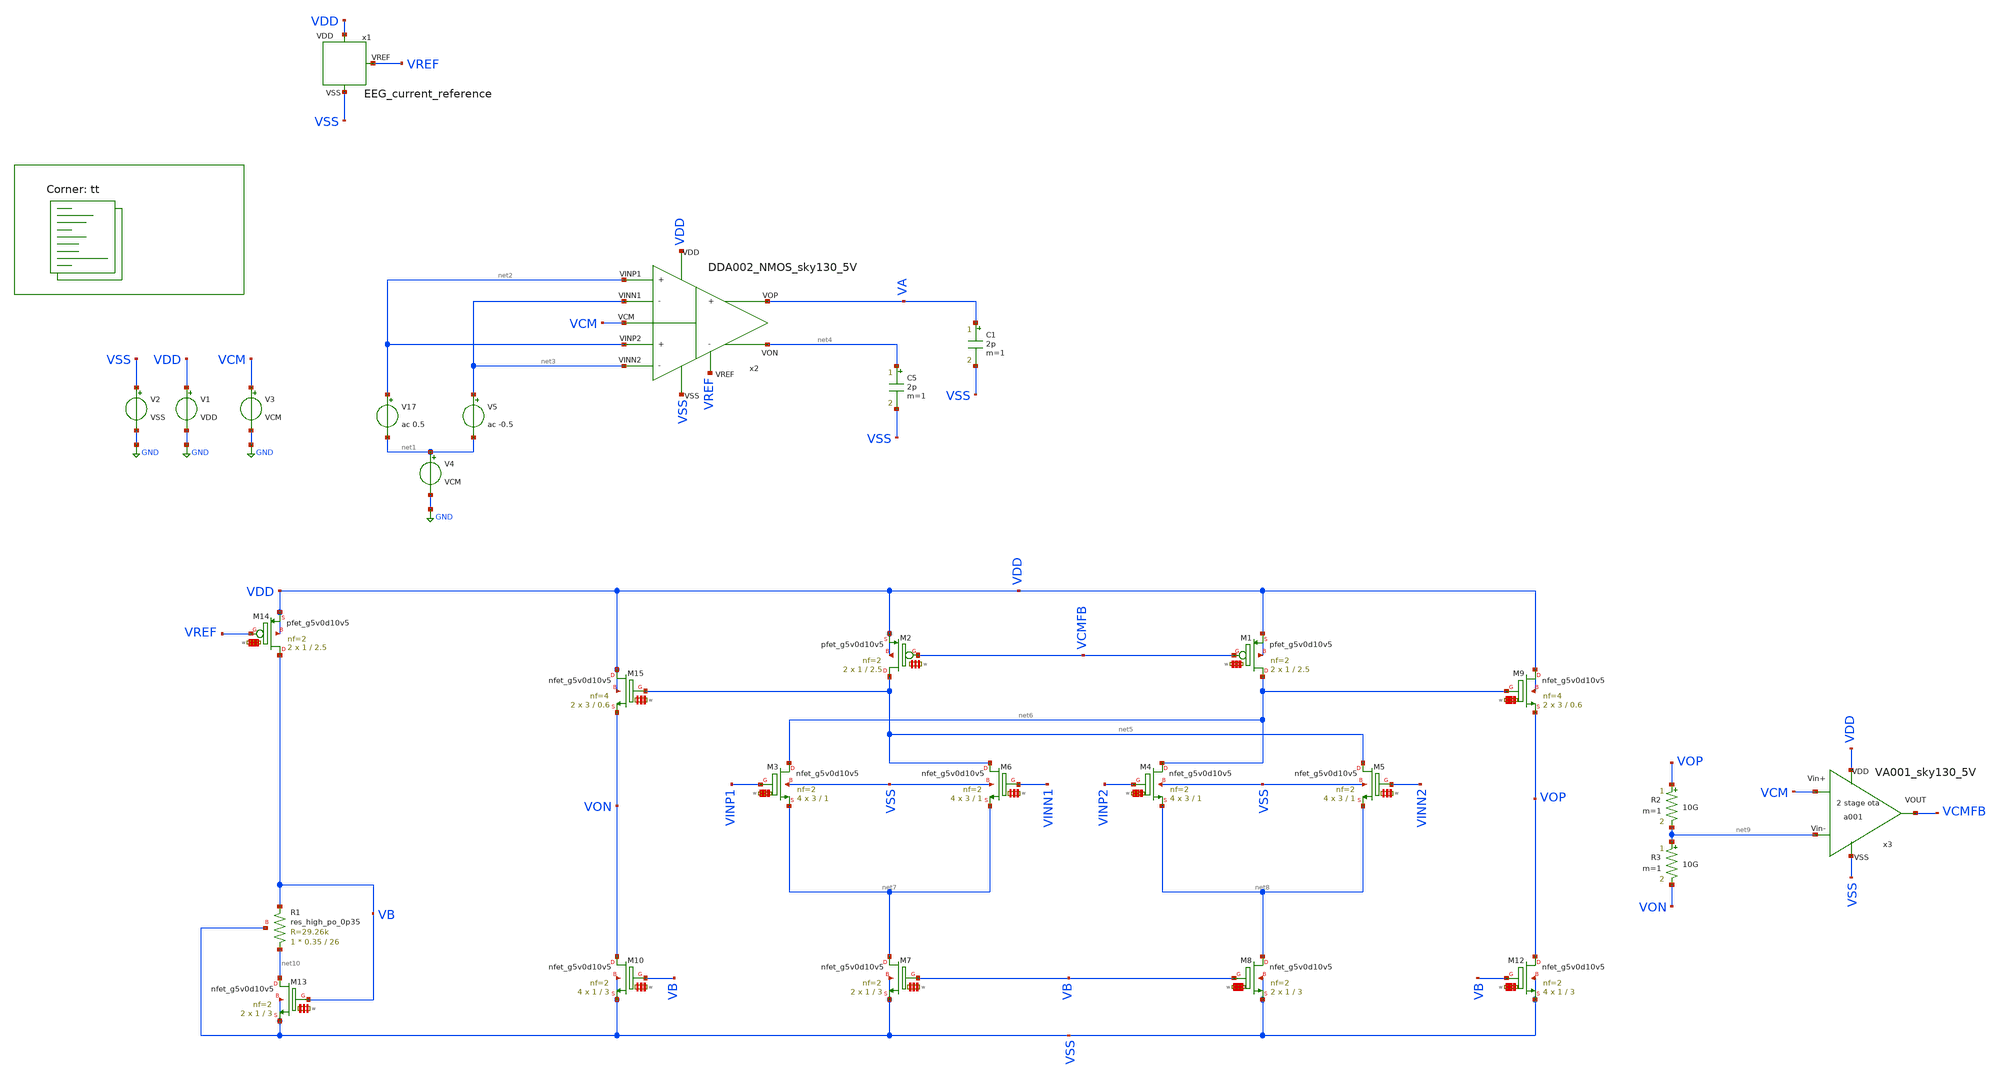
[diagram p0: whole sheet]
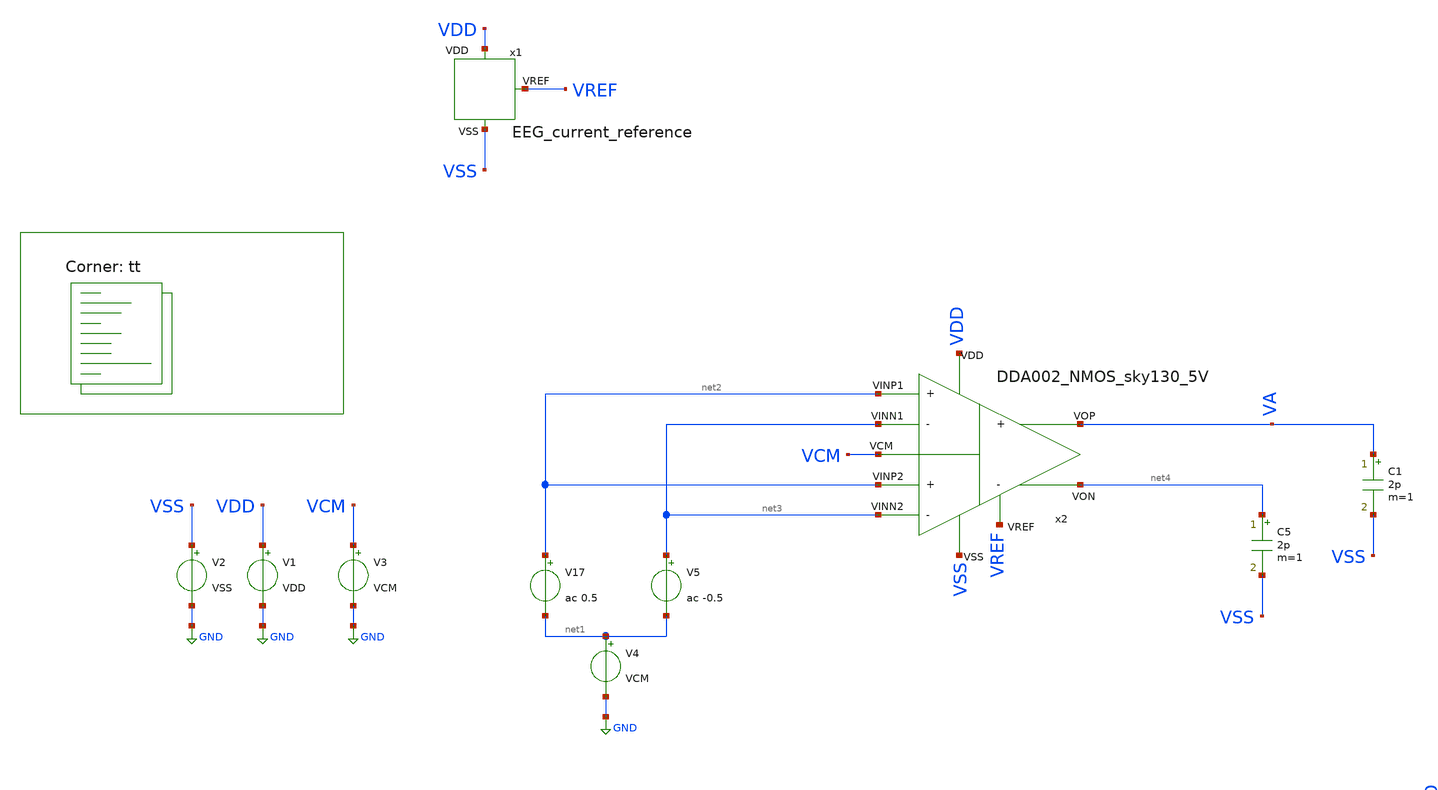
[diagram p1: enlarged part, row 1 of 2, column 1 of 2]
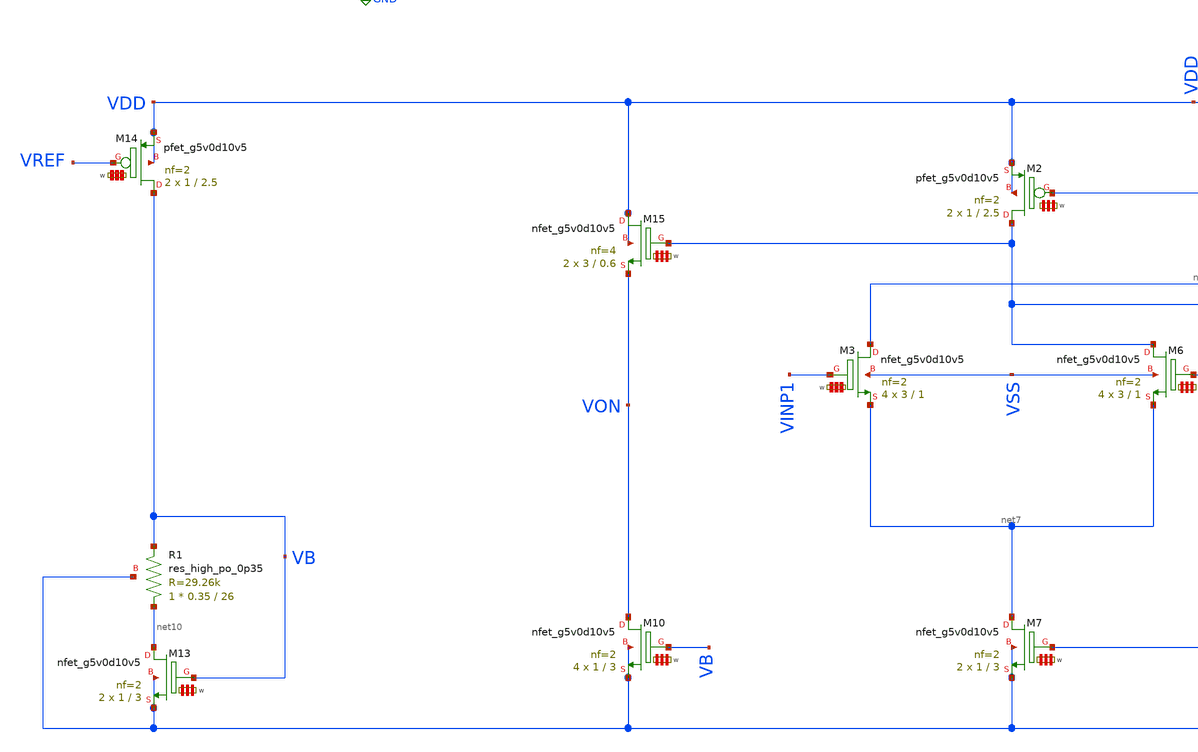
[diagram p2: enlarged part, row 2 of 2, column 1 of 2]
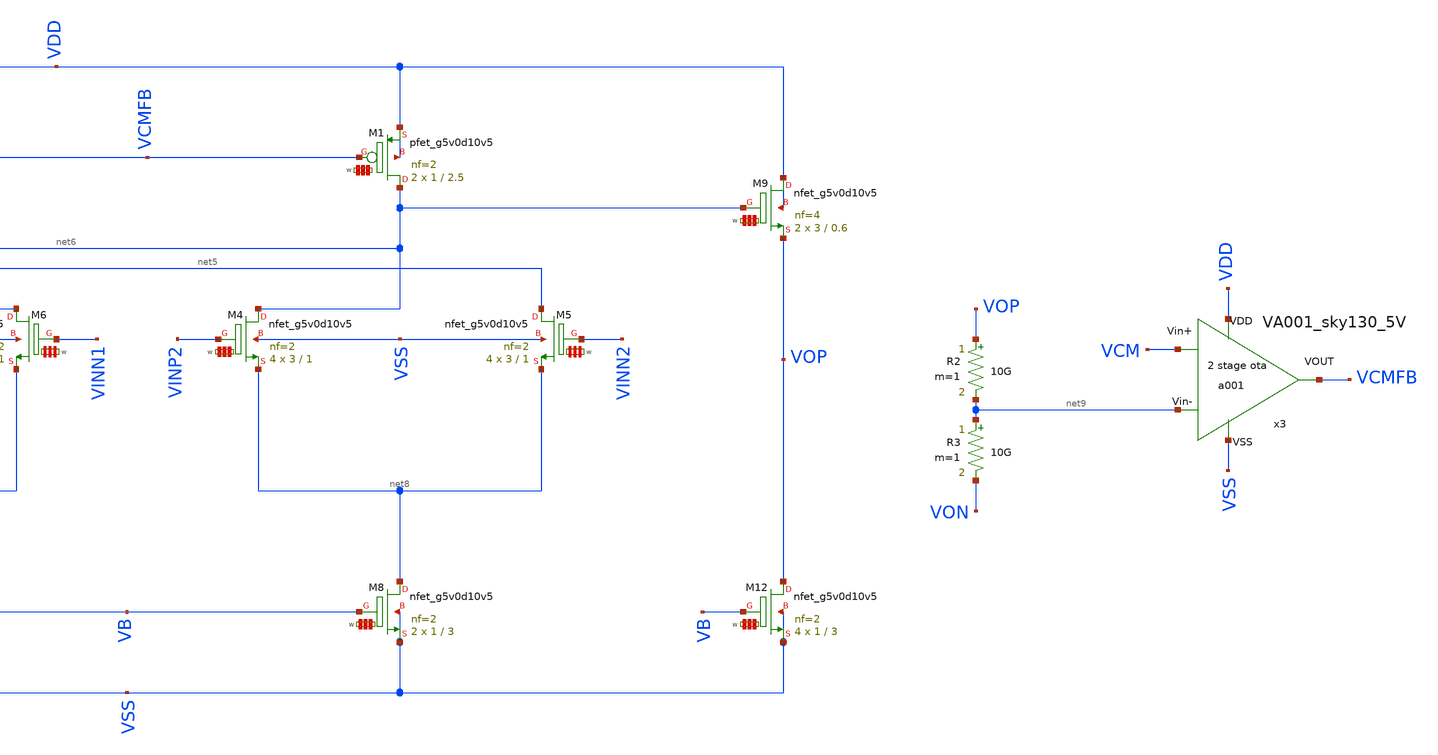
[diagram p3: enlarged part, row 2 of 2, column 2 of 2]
** sch_path: Learning/complex_projects/A_Two-Stage_Time_Division_Multiplexing_AFE_with_Input_Impedance_Boosting_DDA_for_EEG_Signal_Acquisition/sky130A_5V/input_buffer_chopper/DDA_TB.sch
**.subckt DDA_TB
V1 VDD GND VDD
V2 VSS GND VSS
x1 VDD VSS VREF EEG_current_reference
x2 VDD VSS VREF net3 net3 net2 net2 VCM VA net4 DDA002_NMOS_sky130_5V
V3 VCM GND VCM
V4 net1 GND VCM
V17 net2 net1 ac 0.5
V5 net3 net1 ac -0.5
C5 net4 VSS 2p m=1
C1 VA VSS 2p m=1
XM2 net5 VCMFB VDD VDD sky130_fd_pr__pfet_g5v0d10v5 L=2.5 W='1 * 2 ' nf=2 ad='int((2 + 1)/2) * 1 * 0.29'
+ as='int((2 + 2)/2) * 1 * 0.29' pd='2*int((2 + 1)/2) * (1 + 0.29)' ps='2*int((2 + 2)/2) * (1 + 0.29)'
+ nrd='0.29 / 1 / 2 ' nrs='0.29 / 1 / 2 ' sa=0 sb=0 sd=0 mult=2 m=2
XM3 net6 VINP1 net7 VSS sky130_fd_pr__nfet_g5v0d10v5 L=1 W='3 * 2 ' nf=2 ad='int((nf+1)/2) * W / nf * 0.29'
+ as='int((nf+2)/2) * W / nf * 0.29' pd='2*int((nf+1)/2) * (W / nf + 0.29)' ps='2*int((nf+2)/2) * (W / nf + 0.29)'
+ nrd='0.29 / W ' nrs='0.29 / W ' sa=0 sb=0 sd=0 mult=4 m=4
x3 VDD VSS VCM net9 VCMFB VA001_sky130_5V
R2 VOP net9 10G m=1
R3 net9 VON 10G m=1
XM13 net10 VB VSS VSS sky130_fd_pr__nfet_g5v0d10v5 L=3 W='1 * 2 ' nf=2 ad='int((nf+1)/2) * W / nf * 0.29'
+ as='int((nf+2)/2) * W / nf * 0.29' pd='2*int((nf+1)/2) * (W / nf + 0.29)' ps='2*int((nf+2)/2) * (W / nf + 0.29)'
+ nrd='0.29 / W ' nrs='0.29 / W ' sa=0 sb=0 sd=0 mult=2 m=2
XR1 net10 VB VSS sky130_fd_pr__res_high_po_0p35 L=26 mult=1 m=1
XM14 VB VREF VDD VDD sky130_fd_pr__pfet_g5v0d10v5 L=2.5 W='1 * 2 ' nf=2 ad='int((2 + 1)/2) * 1 * 0.29'
+ as='int((2 + 2)/2) * 1 * 0.29' pd='2*int((2 + 1)/2) * (1 + 0.29)' ps='2*int((2 + 2)/2) * (1 + 0.29)'
+ nrd='0.29 / 1 / 2 ' nrs='0.29 / 1 / 2 ' sa=0 sb=0 sd=0 mult=2 m=2
XM7 net7 VB VSS VSS sky130_fd_pr__nfet_g5v0d10v5 L=3 W='1 * 2 ' nf=2 ad='int((nf+1)/2) * W / nf * 0.29'
+ as='int((nf+2)/2) * W / nf * 0.29' pd='2*int((nf+1)/2) * (W / nf + 0.29)' ps='2*int((nf+2)/2) * (W / nf + 0.29)'
+ nrd='0.29 / W ' nrs='0.29 / W ' sa=0 sb=0 sd=0 mult=2 m=2
XM8 net8 VB VSS VSS sky130_fd_pr__nfet_g5v0d10v5 L=3 W='1 * 2 ' nf=2 ad='int((nf+1)/2) * W / nf * 0.29'
+ as='int((nf+2)/2) * W / nf * 0.29' pd='2*int((nf+1)/2) * (W / nf + 0.29)' ps='2*int((nf+2)/2) * (W / nf + 0.29)'
+ nrd='0.29 / W ' nrs='0.29 / W ' sa=0 sb=0 sd=0 mult=2 m=2
XM10 VON VB VSS VSS sky130_fd_pr__nfet_g5v0d10v5 L=3 W='1 * 2 ' nf=2 ad='int((nf+1)/2) * W / nf * 0.29'
+ as='int((nf+2)/2) * W / nf * 0.29' pd='2*int((nf+1)/2) * (W / nf + 0.29)' ps='2*int((nf+2)/2) * (W / nf + 0.29)'
+ nrd='0.29 / W ' nrs='0.29 / W ' sa=0 sb=0 sd=0 mult=4 m=4
XM12 VOP VB VSS VSS sky130_fd_pr__nfet_g5v0d10v5 L=3 W='1 * 2 ' nf=2 ad='int((nf+1)/2) * W / nf * 0.29'
+ as='int((nf+2)/2) * W / nf * 0.29' pd='2*int((nf+1)/2) * (W / nf + 0.29)' ps='2*int((nf+2)/2) * (W / nf + 0.29)'
+ nrd='0.29 / W ' nrs='0.29 / W ' sa=0 sb=0 sd=0 mult=4 m=4
XM6 net5 VINN1 net7 VSS sky130_fd_pr__nfet_g5v0d10v5 L=1 W='3 * 2 ' nf=2 ad='int((nf+1)/2) * W / nf * 0.29'
+ as='int((nf+2)/2) * W / nf * 0.29' pd='2*int((nf+1)/2) * (W / nf + 0.29)' ps='2*int((nf+2)/2) * (W / nf + 0.29)'
+ nrd='0.29 / W ' nrs='0.29 / W ' sa=0 sb=0 sd=0 mult=4 m=4
XM4 net6 VINP2 net8 VSS sky130_fd_pr__nfet_g5v0d10v5 L=1 W='3 * 2 ' nf=2 ad='int((nf+1)/2) * W / nf * 0.29'
+ as='int((nf+2)/2) * W / nf * 0.29' pd='2*int((nf+1)/2) * (W / nf + 0.29)' ps='2*int((nf+2)/2) * (W / nf + 0.29)'
+ nrd='0.29 / W ' nrs='0.29 / W ' sa=0 sb=0 sd=0 mult=4 m=4
XM5 net5 VINN2 net8 VSS sky130_fd_pr__nfet_g5v0d10v5 L=1 W='3 * 2 ' nf=2 ad='int((nf+1)/2) * W / nf * 0.29'
+ as='int((nf+2)/2) * W / nf * 0.29' pd='2*int((nf+1)/2) * (W / nf + 0.29)' ps='2*int((nf+2)/2) * (W / nf + 0.29)'
+ nrd='0.29 / W ' nrs='0.29 / W ' sa=0 sb=0 sd=0 mult=4 m=4
XM1 net6 VCMFB VDD VDD sky130_fd_pr__pfet_g5v0d10v5 L=2.5 W='1 * 2 ' nf=2 ad='int((2 + 1)/2) * 1 * 0.29'
+ as='int((2 + 2)/2) * 1 * 0.29' pd='2*int((2 + 1)/2) * (1 + 0.29)' ps='2*int((2 + 2)/2) * (1 + 0.29)'
+ nrd='0.29 / 1 / 2 ' nrs='0.29 / 1 / 2 ' sa=0 sb=0 sd=0 mult=2 m=2
XM15 VDD net5 VON VDD sky130_fd_pr__nfet_g5v0d10v5 L=0.6 W='3 * 4 ' nf=4 ad='int((nf+1)/2) * W / nf * 0.29'
+ as='int((nf+2)/2) * W / nf * 0.29' pd='2*int((nf+1)/2) * (W / nf + 0.29)' ps='2*int((nf+2)/2) * (W / nf + 0.29)'
+ nrd='0.29 / W ' nrs='0.29 / W ' sa=0 sb=0 sd=0 mult=2 m=2
XM9 VDD net6 VOP VDD sky130_fd_pr__nfet_g5v0d10v5 L=0.6 W='3 * 4 ' nf=4 ad='int((nf+1)/2) * W / nf * 0.29'
+ as='int((nf+2)/2) * W / nf * 0.29' pd='2*int((nf+1)/2) * (W / nf + 0.29)' ps='2*int((nf+2)/2) * (W / nf + 0.29)'
+ nrd='0.29 / W ' nrs='0.29 / W ' sa=0 sb=0 sd=0 mult=2 m=2
**** begin user architecture code
.lib $::SKYWATER_MODELS/sky130.lib.spice tt

.Temp 27
.param VDD = 5
.param VSS = 0
.param CL = 3p
.param V_OFF = -400u
.param VCM = 2.5


.control

	save all
	ac dec 100 1 10G
	plot db(v(VA)) (180+(180*ph(v(VA))/pi))
	op
	print v(VA)

.endc




**** end user architecture code
**.ends
.GLOBAL GND
.end
